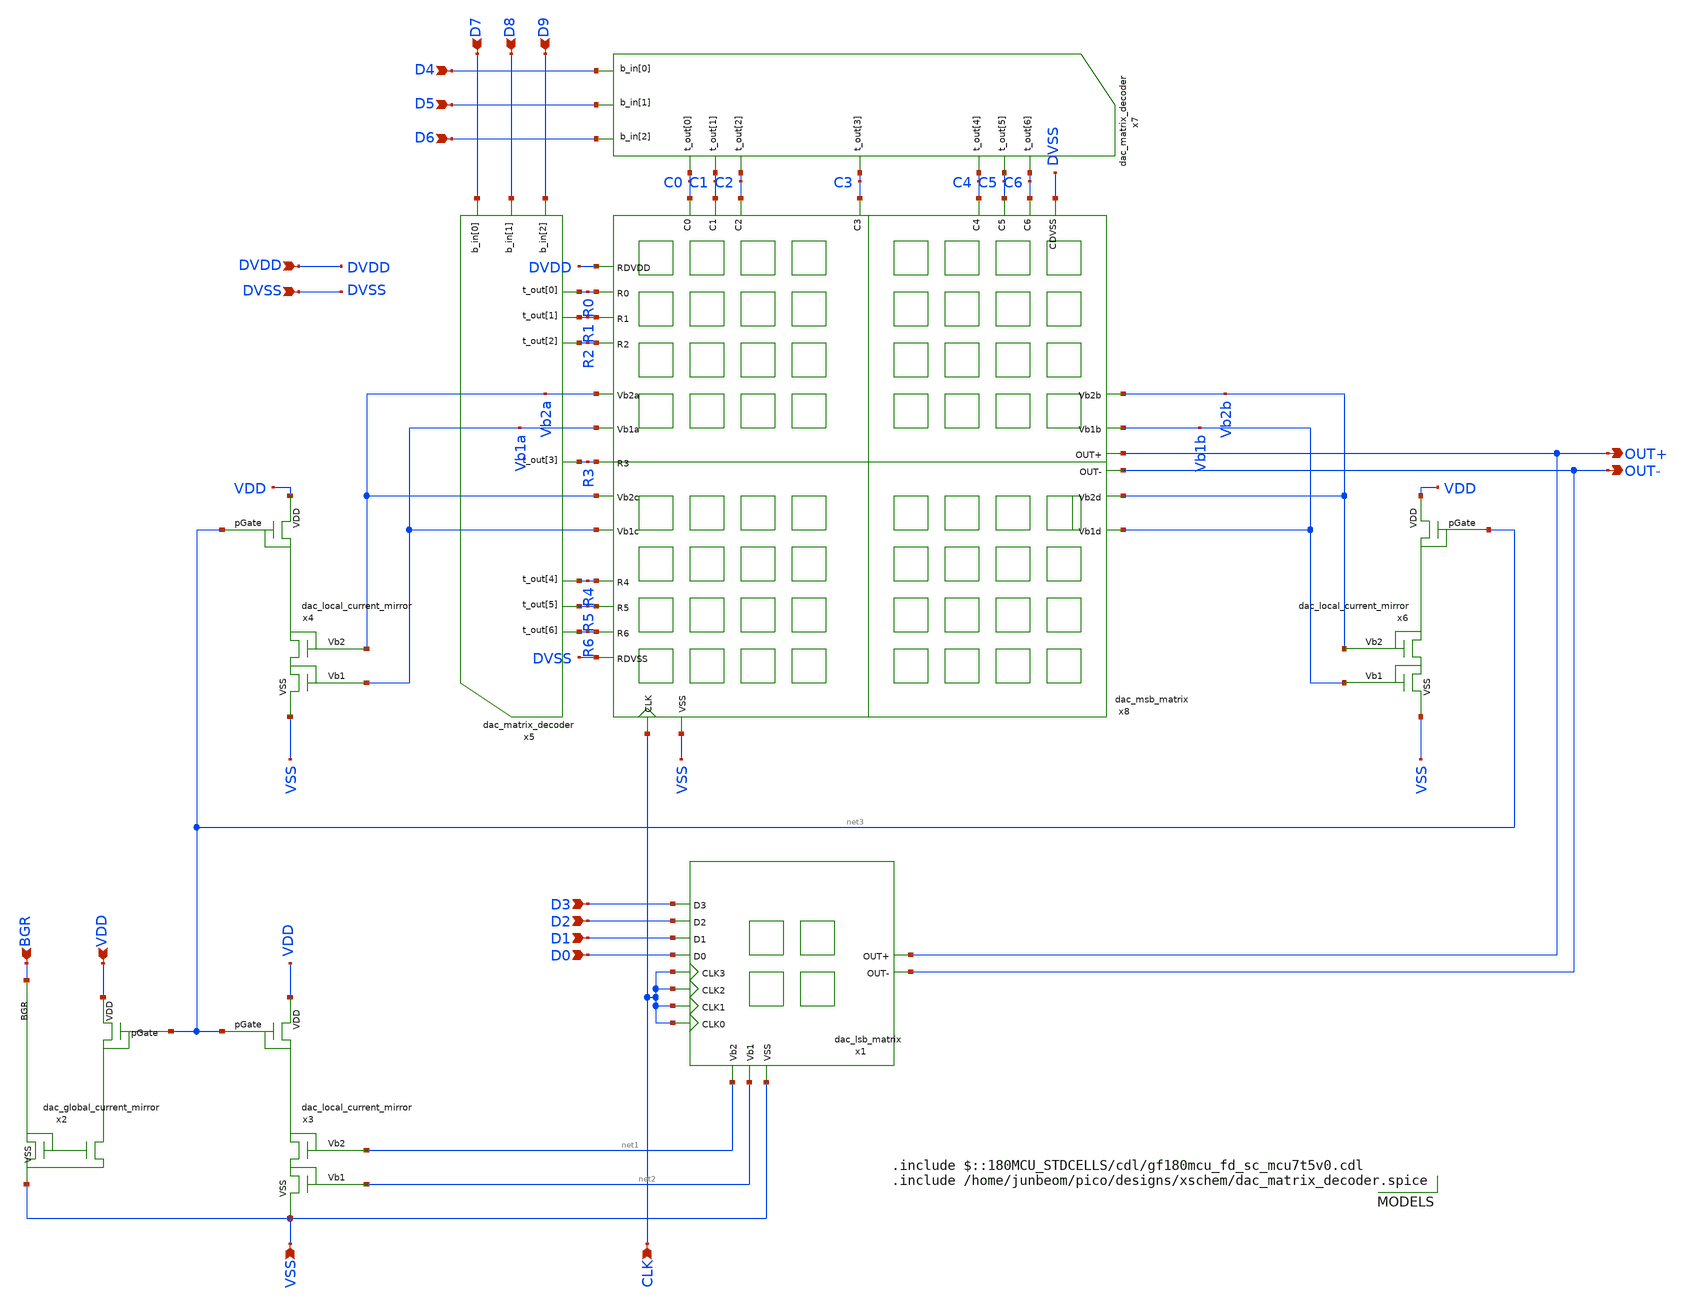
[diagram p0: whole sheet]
** sch_path: DAC/xschem/dac_top.sch
**.subckt dac_top BGR VDD VSS CLK OUT+ OUT- D0 D1 D2 D3 D7 D8 D9 D4 D5 D6 DVDD DVSS
*.ipin BGR
*.ipin VDD
*.ipin VSS
*.ipin CLK
*.opin OUT+
*.opin OUT-
*.ipin D0
*.ipin D1
*.ipin D2
*.ipin D3
*.ipin D7
*.ipin D8
*.ipin D9
*.ipin D4
*.ipin D5
*.ipin D6
*.ipin DVDD
*.ipin DVSS
x2 VDD net3 BGR VSS dac_global_current_mirror
x3 VDD net3 net1 net2 VSS dac_local_current_mirror
x4 VDD net3 Vb2a Vb1a VSS dac_local_current_mirror
x6 VDD net3 Vb2b Vb1b VSS dac_local_current_mirror
x1 D3 D2 D1 D0 CLK CLK CLK CLK net1 net2 VSS OUT+ OUT- DVDD DVSS dac_lsb_matrix
x8 DVDD R0 R1 R2 R3 R4 R5 R6 DVSS C0 C1 C2 C3 C4 C5 C6 DVSS Vb2a Vb1a Vb2a Vb1a Vb2b Vb1b Vb2b Vb1b
+ CLK VSS OUT+ OUT- DVDD DVSS dac_msb_matrix
x5 D7 D8 D9 R0 R1 R2 R3 R4 R5 R6 DVDD DVSS dac_matrix_decoder
x7 D4 D5 D6 C0 C1 C2 C3 C4 C5 C6 DVDD DVSS dac_matrix_decoder
**** begin user architecture code

.include $::180MCU_STDCELLS/cdl/gf180mcu_fd_sc_mcu7t5v0.cdl
.include /home/junbeom/pico/designs/xschem/dac_matrix_decoder.spice

**** end user architecture code
**.ends

* expanding   symbol:  dac_global_current_mirror.sym # of pins=4
** sym_path: DAC/xschem/dac_global_current_mirror.sym
** sch_path: DAC/xschem/dac_global_current_mirror.sch
.subckt dac_global_current_mirror VDD pGate BGR VSS
*.ipin BGR
*.ipin VDD
*.opin pGate
*.ipin VSS
XM1 pGate pGate VDD VDD pfet_03v3 L=1u W=1u nf=1 ad='int((nf+1)/2) * W/nf * 0.18u' as='int((nf+2)/2) * W/nf * 0.18u'
+ pd='2*int((nf+1)/2) * (W/nf + 0.18u)' ps='2*int((nf+2)/2) * (W/nf + 0.18u)' nrd='0.18u / W' nrs='0.18u / W'
+ sa=0 sb=0 sd=0 m=1
XMN1 BGR BGR VSS VSS nfet_03v3 L=4u W=1u nf=4 ad='int((nf+1)/2) * W/nf * 0.18u' as='int((nf+2)/2) * W/nf * 0.18u'
+ pd='2*int((nf+1)/2) * (W/nf + 0.18u)' ps='2*int((nf+2)/2) * (W/nf + 0.18u)' nrd='0.18u / W' nrs='0.18u / W'
+ sa=0 sb=0 sd=0 m=1
XMN2 pGate BGR VSS VSS nfet_03v3 L=4u W=1u nf=4 ad='int((nf+1)/2) * W/nf * 0.18u' as='int((nf+2)/2) * W/nf * 0.18u'
+ pd='2*int((nf+1)/2) * (W/nf + 0.18u)' ps='2*int((nf+2)/2) * (W/nf + 0.18u)' nrd='0.18u / W' nrs='0.18u / W'
+ sa=0 sb=0 sd=0 m=1
.ends


* expanding   symbol:  dac_local_current_mirror.sym # of pins=5
** sym_path: DAC/xschem/dac_local_current_mirror.sym
** sch_path: DAC/xschem/dac_local_current_mirror.sch
.subckt dac_local_current_mirror VDD pGate Vb2 Vb1 VSS
*.ipin VSS
*.opin Vb2
*.opin Vb1
*.ipin VDD
*.ipin pGate
XM2 Vb2 pGate VDD VDD pfet_03v3 L=1u W=5u nf=5 ad='int((nf+1)/2) * W/nf * 0.18u' as='int((nf+2)/2) * W/nf * 0.18u'
+ pd='2*int((nf+1)/2) * (W/nf + 0.18u)' ps='2*int((nf+2)/2) * (W/nf + 0.18u)' nrd='0.18u / W' nrs='0.18u / W'
+ sa=0 sb=0 sd=0 m=1
XM5 Vb2 Vb2 Vb1 VSS nfet_03v3 L=1u W=4u nf=4 ad='int((nf+1)/2) * W/nf * 0.18u' as='int((nf+2)/2) * W/nf * 0.18u'
+ pd='2*int((nf+1)/2) * (W/nf + 0.18u)' ps='2*int((nf+2)/2) * (W/nf + 0.18u)' nrd='0.18u / W' nrs='0.18u / W'
+ sa=0 sb=0 sd=0 m=1
XM6 Vb1 Vb1 VSS VSS nfet_03v3 L=1u W=4u nf=4 ad='int((nf+1)/2) * W/nf * 0.18u' as='int((nf+2)/2) * W/nf * 0.18u'
+ pd='2*int((nf+1)/2) * (W/nf + 0.18u)' ps='2*int((nf+2)/2) * (W/nf + 0.18u)' nrd='0.18u / W' nrs='0.18u / W'
+ sa=0 sb=0 sd=0 m=1
.ends


* expanding   symbol:  dac_lsb_matrix.sym # of pins=13
** sym_path: DAC/xschem/dac_lsb_matrix.sym
** sch_path: DAC/xschem/dac_lsb_matrix.sch
.subckt dac_lsb_matrix D3 D2 D1 D0 CLK3 CLK2 CLK1 CLK0 Vb2 Vb1 VSS OUT+ OUT- DVDD DVSS
*.ipin D3
*.ipin D2
*.ipin D1
*.ipin D0
*.ipin CLK3
*.ipin CLK2
*.ipin CLK1
*.ipin CLK0
*.ipin VSS
*.ipin Vb2
*.ipin Vb1
*.opin OUT+
*.opin OUT-
x1 OUT+ OUT- net4 net1 net6 net3 net2 net7 net8 net5 Vb2 Vb1 VSS dac_lsb_analog
x6 D3 CLK3 net1 DVDD DVDD DVSS DVSS gf180mcu_fd_sc_mcu7t5v0__dffq_1
x7 net1 net2 DVDD DVDD DVSS DVSS gf180mcu_fd_sc_mcu7t5v0__inv_1
x4 D2 CLK2 net3 DVDD DVDD DVSS DVSS gf180mcu_fd_sc_mcu7t5v0__dffq_1
x5 net3 net4 DVDD DVDD DVSS DVSS gf180mcu_fd_sc_mcu7t5v0__inv_1
x3 D1 CLK1 net7 DVDD DVDD DVSS DVSS gf180mcu_fd_sc_mcu7t5v0__dffq_1
x8 net7 net6 DVDD DVDD DVSS DVSS gf180mcu_fd_sc_mcu7t5v0__inv_1
x2 D0 CLK0 net5 DVDD DVDD DVSS DVSS gf180mcu_fd_sc_mcu7t5v0__dffq_1
x9 net5 net8 DVDD DVDD DVSS DVSS gf180mcu_fd_sc_mcu7t5v0__inv_1
.ends


* expanding   symbol:  dac_msb_matrix.sym # of pins=29
** sym_path: DAC/xschem/dac_msb_matrix.sym
** sch_path: DAC/xschem/dac_msb_matrix.sch
.subckt dac_msb_matrix RDVDD R0 R1 R2 R3 R4 R5 R6 RDVSS C0 C1 C2 C3 C4 C5 C6 CDVSS Vb2a Vb1a Vb2c
+ Vb1c Vb2b Vb1b Vb2d Vb1d CLK VSS OUT+ OUT- DVDD DVSS
*.ipin R0
*.ipin R1
*.ipin R2
*.ipin R3
*.ipin R4
*.ipin R5
*.ipin R6
*.ipin C0
*.ipin C1
*.ipin C2
*.ipin C3
*.ipin C4
*.ipin C5
*.ipin C6
*.ipin VSS
*.ipin Vb2a
*.ipin Vb1a
*.ipin Vb2b
*.ipin Vb1b
*.ipin Vb2c
*.ipin Vb1c
*.ipin Vb2d
*.ipin Vb1d
*.opin OUT+
*.opin OUT-
*.ipin CLK
*.ipin RDVDD
*.ipin RDVSS
*.ipin CDVSS
x1 R3 R4 R4 R5 R5 R6 R6 RDVSS C0 C1 C2 C3 CLK Vb2c Vb1c VSS OUT+ OUT- DVDD DVSS
+ dac_msb_quarter_matrix
x3 R3 R4 R4 R5 R5 R6 R6 RDVSS C4 C5 C6 CDVSS CLK Vb2d Vb1d VSS OUT+ OUT- DVDD DVSS
+ dac_msb_quarter_matrix
x4 RDVDD R0 R0 R1 R1 R2 R2 R3 C4 C5 C6 CDVSS CLK Vb2b Vb1b VSS OUT+ OUT- DVDD DVSS
+ dac_msb_quarter_matrix
x5 RDVDD R0 R0 R1 R1 R2 R2 R3 C0 C1 C2 C3 CLK Vb2a Vb1a VSS OUT+ OUT- DVDD DVSS
+ dac_msb_quarter_matrix
.ends


* expanding   symbol:  dac_lsb_analog.sym # of pins=13
** sym_path: DAC/xschem/dac_lsb_analog.sym
** sch_path: DAC/xschem/dac_lsb_analog.sch
.subckt dac_lsb_analog OUT+ OUT- Q2- Q3+ Q1- Q2+ Q3- Q1+ Q0- Q0+ Vb2 Vb1 VSS
*.ipin VSS
*.ipin Vb2
*.ipin Vb1
*.ipin Q3-
*.ipin Q3+
*.ipin Q2-
*.ipin Q2+
*.ipin Q1-
*.ipin Q1+
*.ipin Q0-
*.ipin Q0+
*.opin OUT+
*.opin OUT-
XM7 net1 Vb2 net2 VSS nfet_03v3 L=0.5u W=2u nf=2 ad='int((nf+1)/2) * W/nf * 0.18u' as='int((nf+2)/2) * W/nf * 0.18u'
+ pd='2*int((nf+1)/2) * (W/nf + 0.18u)' ps='2*int((nf+2)/2) * (W/nf + 0.18u)' nrd='0.18u / W' nrs='0.18u / W'
+ sa=0 sb=0 sd=0 m=1
XM8 net2 Vb1 VSS VSS nfet_03v3 L=0.5u W=2u nf=1 ad='int((nf+1)/2) * W/nf * 0.18u' as='int((nf+2)/2) * W/nf * 0.18u'
+ pd='2*int((nf+1)/2) * (W/nf + 0.18u)' ps='2*int((nf+2)/2) * (W/nf + 0.18u)' nrd='0.18u / W' nrs='0.18u / W'
+ sa=0 sb=0 sd=0 m=1
XM12 OUT+ Q0+ net1 VSS nfet_03v3 L=0.5u W=1u nf=1 ad='int((nf+1)/2) * W/nf * 0.18u' as='int((nf+2)/2) * W/nf * 0.18u'
+ pd='2*int((nf+1)/2) * (W/nf + 0.18u)' ps='2*int((nf+2)/2) * (W/nf + 0.18u)' nrd='0.18u / W' nrs='0.18u / W'
+ sa=0 sb=0 sd=0 m=1
XM13 OUT- Q0- net1 VSS nfet_03v3 L=0.5u W=1u nf=1 ad='int((nf+1)/2) * W/nf * 0.18u' as='int((nf+2)/2) * W/nf * 0.18u'
+ pd='2*int((nf+1)/2) * (W/nf + 0.18u)' ps='2*int((nf+2)/2) * (W/nf + 0.18u)' nrd='0.18u / W' nrs='0.18u / W'
+ sa=0 sb=0 sd=0 m=1
XM14 net3 Vb2 net4 VSS nfet_03v3 L=0.5u W=4u nf=4 ad='int((nf+1)/2) * W/nf * 0.18u' as='int((nf+2)/2) * W/nf * 0.18u'
+ pd='2*int((nf+1)/2) * (W/nf + 0.18u)' ps='2*int((nf+2)/2) * (W/nf + 0.18u)' nrd='0.18u / W' nrs='0.18u / W'
+ sa=0 sb=0 sd=0 m=1
XM15 net4 Vb1 VSS VSS nfet_03v3 L=0.5u W=4u nf=2 ad='int((nf+1)/2) * W/nf * 0.18u' as='int((nf+2)/2) * W/nf * 0.18u'
+ pd='2*int((nf+1)/2) * (W/nf + 0.18u)' ps='2*int((nf+2)/2) * (W/nf + 0.18u)' nrd='0.18u / W' nrs='0.18u / W'
+ sa=0 sb=0 sd=0 m=1
XM18 OUT+ Q1+ net3 VSS nfet_03v3 L=0.5u W=2u nf=2 ad='int((nf+1)/2) * W/nf * 0.18u' as='int((nf+2)/2) * W/nf * 0.18u'
+ pd='2*int((nf+1)/2) * (W/nf + 0.18u)' ps='2*int((nf+2)/2) * (W/nf + 0.18u)' nrd='0.18u / W' nrs='0.18u / W'
+ sa=0 sb=0 sd=0 m=1
XM19 OUT- Q1- net3 VSS nfet_03v3 L=0.5u W=2u nf=2 ad='int((nf+1)/2) * W/nf * 0.18u' as='int((nf+2)/2) * W/nf * 0.18u'
+ pd='2*int((nf+1)/2) * (W/nf + 0.18u)' ps='2*int((nf+2)/2) * (W/nf + 0.18u)' nrd='0.18u / W' nrs='0.18u / W'
+ sa=0 sb=0 sd=0 m=1
XM20 net5 Vb2 net6 VSS nfet_03v3 L=0.5u W=8u nf=8 ad='int((nf+1)/2) * W/nf * 0.18u' as='int((nf+2)/2) * W/nf * 0.18u'
+ pd='2*int((nf+1)/2) * (W/nf + 0.18u)' ps='2*int((nf+2)/2) * (W/nf + 0.18u)' nrd='0.18u / W' nrs='0.18u / W'
+ sa=0 sb=0 sd=0 m=1
XM21 net6 Vb1 VSS VSS nfet_03v3 L=0.5u W=8u nf=4 ad='int((nf+1)/2) * W/nf * 0.18u' as='int((nf+2)/2) * W/nf * 0.18u'
+ pd='2*int((nf+1)/2) * (W/nf + 0.18u)' ps='2*int((nf+2)/2) * (W/nf + 0.18u)' nrd='0.18u / W' nrs='0.18u / W'
+ sa=0 sb=0 sd=0 m=1
XM24 OUT+ Q2+ net5 VSS nfet_03v3 L=0.5u W=4u nf=4 ad='int((nf+1)/2) * W/nf * 0.18u' as='int((nf+2)/2) * W/nf * 0.18u'
+ pd='2*int((nf+1)/2) * (W/nf + 0.18u)' ps='2*int((nf+2)/2) * (W/nf + 0.18u)' nrd='0.18u / W' nrs='0.18u / W'
+ sa=0 sb=0 sd=0 m=1
XM25 OUT- Q2- net5 VSS nfet_03v3 L=0.5u W=4u nf=4 ad='int((nf+1)/2) * W/nf * 0.18u' as='int((nf+2)/2) * W/nf * 0.18u'
+ pd='2*int((nf+1)/2) * (W/nf + 0.18u)' ps='2*int((nf+2)/2) * (W/nf + 0.18u)' nrd='0.18u / W' nrs='0.18u / W'
+ sa=0 sb=0 sd=0 m=1
XM26 net7 Vb2 net8 VSS nfet_03v3 L=0.5u W=16u nf=16 ad='int((nf+1)/2) * W/nf * 0.18u' as='int((nf+2)/2) * W/nf * 0.18u'
+ pd='2*int((nf+1)/2) * (W/nf + 0.18u)' ps='2*int((nf+2)/2) * (W/nf + 0.18u)' nrd='0.18u / W' nrs='0.18u / W'
+ sa=0 sb=0 sd=0 m=1
XM27 net8 Vb1 VSS VSS nfet_03v3 L=0.5u W=16u nf=8 ad='int((nf+1)/2) * W/nf * 0.18u' as='int((nf+2)/2) * W/nf * 0.18u'
+ pd='2*int((nf+1)/2) * (W/nf + 0.18u)' ps='2*int((nf+2)/2) * (W/nf + 0.18u)' nrd='0.18u / W' nrs='0.18u / W'
+ sa=0 sb=0 sd=0 m=1
XM30 OUT+ Q3+ net7 VSS nfet_03v3 L=0.5u W=8u nf=8 ad='int((nf+1)/2) * W/nf * 0.18u' as='int((nf+2)/2) * W/nf * 0.18u'
+ pd='2*int((nf+1)/2) * (W/nf + 0.18u)' ps='2*int((nf+2)/2) * (W/nf + 0.18u)' nrd='0.18u / W' nrs='0.18u / W'
+ sa=0 sb=0 sd=0 m=1
XM31 OUT- Q3- net7 VSS nfet_03v3 L=0.5u W=8u nf=8 ad='int((nf+1)/2) * W/nf * 0.18u' as='int((nf+2)/2) * W/nf * 0.18u'
+ pd='2*int((nf+1)/2) * (W/nf + 0.18u)' ps='2*int((nf+2)/2) * (W/nf + 0.18u)' nrd='0.18u / W' nrs='0.18u / W'
+ sa=0 sb=0 sd=0 m=1
.ends


* expanding   symbol:  dac_msb_quarter_matrix.sym # of pins=18
** sym_path: DAC/xschem/dac_msb_quarter_matrix.sym
** sch_path: DAC/xschem/dac_msb_quarter_matrix.sch
.subckt dac_msb_quarter_matrix R0 R1 R2 R3 R4 R5 R6 R7 C0 C1 C2 C3 CLK Vb2 Vb1 VSS OUT+ OUT- DVDD
+ DVSS
*.ipin CLK
*.ipin R0
*.ipin R1
*.ipin R2
*.ipin R3
*.ipin R4
*.ipin R5
*.ipin R6
*.ipin R7
*.ipin C0
*.ipin C1
*.ipin C2
*.ipin C3
*.ipin VSS
*.ipin Vb2
*.ipin Vb1
*.opin OUT+
*.opin OUT-
x13 C0 R6 R7 CLK Vb2 Vb1 VSS OUT+ OUT- DVDD DVSS dac_msb_cell
x1 C1 R6 R7 CLK Vb2 Vb1 VSS OUT+ OUT- DVDD DVSS dac_msb_cell
x3 C2 R6 R7 CLK Vb2 Vb1 VSS OUT+ OUT- DVDD DVSS dac_msb_cell
x5 C3 R6 R7 CLK Vb2 Vb1 VSS OUT+ OUT- DVDD DVSS dac_msb_cell
x2 C0 R4 R5 CLK Vb2 Vb1 VSS OUT+ OUT- DVDD DVSS dac_msb_cell
x4 C1 R4 R5 CLK Vb2 Vb1 VSS OUT+ OUT- DVDD DVSS dac_msb_cell
x6 C2 R4 R5 CLK Vb2 Vb1 VSS OUT+ OUT- DVDD DVSS dac_msb_cell
x7 C3 R4 R5 CLK Vb2 Vb1 VSS OUT+ OUT- DVDD DVSS dac_msb_cell
x8 C0 R2 R3 CLK Vb2 Vb1 VSS OUT+ OUT- DVDD DVSS dac_msb_cell
x9 C1 R2 R3 CLK Vb2 Vb1 VSS OUT+ OUT- DVDD DVSS dac_msb_cell
x10 C2 R2 R3 CLK Vb2 Vb1 VSS OUT+ OUT- DVDD DVSS dac_msb_cell
x11 C3 R2 R3 CLK Vb2 Vb1 VSS OUT+ OUT- DVDD DVSS dac_msb_cell
x12 C0 R0 R1 CLK Vb2 Vb1 VSS OUT+ OUT- DVDD DVSS dac_msb_cell
x14 C1 R0 R1 CLK Vb2 Vb1 VSS OUT+ OUT- DVDD DVSS dac_msb_cell
x15 C2 R0 R1 CLK Vb2 Vb1 VSS OUT+ OUT- DVDD DVSS dac_msb_cell
x16 C3 R0 R1 CLK Vb2 Vb1 VSS OUT+ OUT- DVDD DVSS dac_msb_cell
.ends


* expanding   symbol:  dac_msb_cell.sym # of pins=9
** sym_path: DAC/xschem/dac_msb_cell.sym
** sch_path: DAC/xschem/dac_msb_cell.sch
.subckt dac_msb_cell Cj Ri Rk CLK Vb2 Vb1 VSS OUT+ OUT- DVDD DVSS
*.ipin Cj
*.ipin Rk
*.ipin Ri
*.ipin CLK
*.ipin Vb2
*.ipin Vb1
*.ipin VSS
*.opin OUT+
*.opin OUT-
x2 net4 CLK net1 DVDD DVDD DVSS DVSS gf180mcu_fd_sc_mcu7t5v0__dffq_1
x3 net1 net2 DVDD DVDD DVSS DVSS gf180mcu_fd_sc_mcu7t5v0__inv_1
x6 Cj Ri net3 DVDD DVDD DVSS DVSS gf180mcu_fd_sc_mcu7t5v0__and2_1
x4 net3 Rk net4 DVDD DVDD DVSS DVSS gf180mcu_fd_sc_mcu7t5v0__or2_1
x1 OUT+ OUT- net2 net1 Vb2 Vb1 VSS dac_msb_analog
.ends


* expanding   symbol:  dac_msb_analog.sym # of pins=7
** sym_path: DAC/xschem/dac_msb_analog.sym
** sch_path: DAC/xschem/dac_msb_analog.sch
.subckt dac_msb_analog OUT+ OUT- Q- Q+ Vb2 Vb1 VSS
*.ipin Q-
*.ipin Q+
*.ipin Vb1
*.ipin Vb2
*.opin OUT+
*.opin OUT-
*.ipin VSS
XM26 net1 Vb2 net2 VSS nfet_03v3 L=0.5u W=32u nf=16 ad='int((nf+1)/2) * W/nf * 0.18u' as='int((nf+2)/2) * W/nf * 0.18u'
+ pd='2*int((nf+1)/2) * (W/nf + 0.18u)' ps='2*int((nf+2)/2) * (W/nf + 0.18u)' nrd='0.18u / W' nrs='0.18u / W'
+ sa=0 sb=0 sd=0 m=1
XM27 net2 Vb1 VSS VSS nfet_03v3 L=0.5u W=32u nf=16 ad='int((nf+1)/2) * W/nf * 0.18u' as='int((nf+2)/2) * W/nf * 0.18u'
+ pd='2*int((nf+1)/2) * (W/nf + 0.18u)' ps='2*int((nf+2)/2) * (W/nf + 0.18u)' nrd='0.18u / W' nrs='0.18u / W'
+ sa=0 sb=0 sd=0 m=1
XM30 OUT+ Q+ net1 VSS nfet_03v3 L=0.5u W=16u nf=8 ad='int((nf+1)/2) * W/nf * 0.18u' as='int((nf+2)/2) * W/nf * 0.18u'
+ pd='2*int((nf+1)/2) * (W/nf + 0.18u)' ps='2*int((nf+2)/2) * (W/nf + 0.18u)' nrd='0.18u / W' nrs='0.18u / W'
+ sa=0 sb=0 sd=0 m=1
XM31 OUT- Q- net1 VSS nfet_03v3 L=0.5u W=16u nf=8 ad='int((nf+1)/2) * W/nf * 0.18u' as='int((nf+2)/2) * W/nf * 0.18u'
+ pd='2*int((nf+1)/2) * (W/nf + 0.18u)' ps='2*int((nf+2)/2) * (W/nf + 0.18u)' nrd='0.18u / W' nrs='0.18u / W'
+ sa=0 sb=0 sd=0 m=1
.ends

.end
